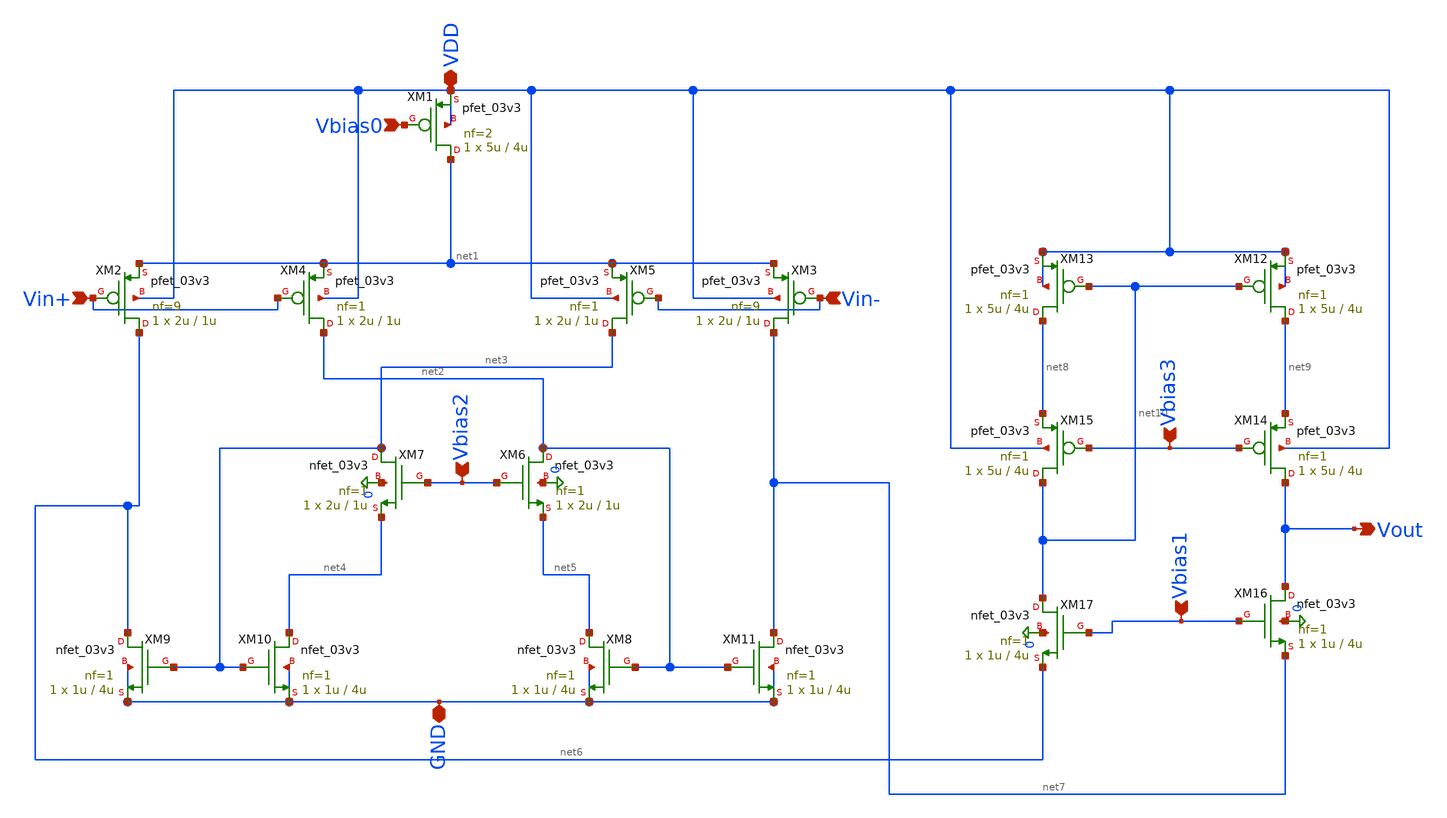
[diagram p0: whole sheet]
** sch_path: analog/folded_cascode_OTA.sch
**.subckt folded_cascode_OTA VDD Vbias0 Vin+ Vin- Vbias1 Vout Vbias3 Vbias2 GND
*.iopin VDD
*.ipin Vbias0
*.ipin Vin+
*.ipin Vin-
*.ipin Vbias1
*.opin Vout
*.ipin Vbias3
*.ipin Vbias2
*.iopin GND
XM1 net1 Vbias0 VDD VDD pfet_03v3 L=4u W=5u nf=2 ad='int((nf+1)/2) * W/nf * 0.18u' as='int((nf+2)/2) * W/nf * 0.18u'
+ pd='2*int((nf+1)/2) * (W/nf + 0.18u)' ps='2*int((nf+2)/2) * (W/nf + 0.18u)' nrd='0.18u / W' nrs='0.18u / W'
+ sa=0 sb=0 sd=0 m=1
XM2 net6 Vin+ net1 VDD pfet_03v3 L=1u W=2u nf=9 ad='int((nf+1)/2) * W/nf * 0.18u' as='int((nf+2)/2) * W/nf * 0.18u'
+ pd='2*int((nf+1)/2) * (W/nf + 0.18u)' ps='2*int((nf+2)/2) * (W/nf + 0.18u)' nrd='0.18u / W' nrs='0.18u / W'
+ sa=0 sb=0 sd=0 m=1
XM3 net7 Vin- net1 VDD pfet_03v3 L=1u W=2u nf=9 ad='int((nf+1)/2) * W/nf * 0.18u' as='int((nf+2)/2) * W/nf * 0.18u'
+ pd='2*int((nf+1)/2) * (W/nf + 0.18u)' ps='2*int((nf+2)/2) * (W/nf + 0.18u)' nrd='0.18u / W' nrs='0.18u / W'
+ sa=0 sb=0 sd=0 m=1
XM4 net2 Vin+ net1 VDD pfet_03v3 L=1u W=2u nf=1 ad='int((nf+1)/2) * W/nf * 0.18u' as='int((nf+2)/2) * W/nf * 0.18u'
+ pd='2*int((nf+1)/2) * (W/nf + 0.18u)' ps='2*int((nf+2)/2) * (W/nf + 0.18u)' nrd='0.18u / W' nrs='0.18u / W'
+ sa=0 sb=0 sd=0 m=1
XM5 net3 Vin- net1 VDD pfet_03v3 L=1u W=2u nf=1 ad='int((nf+1)/2) * W/nf * 0.18u' as='int((nf+2)/2) * W/nf * 0.18u'
+ pd='2*int((nf+1)/2) * (W/nf + 0.18u)' ps='2*int((nf+2)/2) * (W/nf + 0.18u)' nrd='0.18u / W' nrs='0.18u / W'
+ sa=0 sb=0 sd=0 m=1
XM6 net2 Vbias2 net5 0 nfet_03v3 L=1u W=2u nf=1 ad='int((nf+1)/2) * W/nf * 0.18u' as='int((nf+2)/2) * W/nf * 0.18u'
+ pd='2*int((nf+1)/2) * (W/nf + 0.18u)' ps='2*int((nf+2)/2) * (W/nf + 0.18u)' nrd='0.18u / W' nrs='0.18u / W'
+ sa=0 sb=0 sd=0 m=1
XM7 net3 Vbias2 net4 0 nfet_03v3 L=1u W=2u nf=1 ad='int((nf+1)/2) * W/nf * 0.18u' as='int((nf+2)/2) * W/nf * 0.18u'
+ pd='2*int((nf+1)/2) * (W/nf + 0.18u)' ps='2*int((nf+2)/2) * (W/nf + 0.18u)' nrd='0.18u / W' nrs='0.18u / W'
+ sa=0 sb=0 sd=0 m=1
XM8 net5 net2 GND GND nfet_03v3 L=4u W=1u nf=1 ad='int((nf+1)/2) * W/nf * 0.18u' as='int((nf+2)/2) * W/nf * 0.18u'
+ pd='2*int((nf+1)/2) * (W/nf + 0.18u)' ps='2*int((nf+2)/2) * (W/nf + 0.18u)' nrd='0.18u / W' nrs='0.18u / W'
+ sa=0 sb=0 sd=0 m=1
XM9 net6 net3 GND GND nfet_03v3 L=4u W=1u nf=1 ad='int((nf+1)/2) * W/nf * 0.18u' as='int((nf+2)/2) * W/nf * 0.18u'
+ pd='2*int((nf+1)/2) * (W/nf + 0.18u)' ps='2*int((nf+2)/2) * (W/nf + 0.18u)' nrd='0.18u / W' nrs='0.18u / W'
+ sa=0 sb=0 sd=0 m=1
XM10 net4 net3 GND GND nfet_03v3 L=4u W=1u nf=1 ad='int((nf+1)/2) * W/nf * 0.18u' as='int((nf+2)/2) * W/nf * 0.18u'
+ pd='2*int((nf+1)/2) * (W/nf + 0.18u)' ps='2*int((nf+2)/2) * (W/nf + 0.18u)' nrd='0.18u / W' nrs='0.18u / W'
+ sa=0 sb=0 sd=0 m=1
XM11 net7 net2 GND GND nfet_03v3 L=4u W=1u nf=1 ad='int((nf+1)/2) * W/nf * 0.18u' as='int((nf+2)/2) * W/nf * 0.18u'
+ pd='2*int((nf+1)/2) * (W/nf + 0.18u)' ps='2*int((nf+2)/2) * (W/nf + 0.18u)' nrd='0.18u / W' nrs='0.18u / W'
+ sa=0 sb=0 sd=0 m=1
XM12 net9 net10 VDD VDD pfet_03v3 L=4u W=5u nf=1 ad='int((nf+1)/2) * W/nf * 0.18u' as='int((nf+2)/2) * W/nf * 0.18u'
+ pd='2*int((nf+1)/2) * (W/nf + 0.18u)' ps='2*int((nf+2)/2) * (W/nf + 0.18u)' nrd='0.18u / W' nrs='0.18u / W'
+ sa=0 sb=0 sd=0 m=1
XM13 net8 net10 VDD VDD pfet_03v3 L=4u W=5u nf=1 ad='int((nf+1)/2) * W/nf * 0.18u' as='int((nf+2)/2) * W/nf * 0.18u'
+ pd='2*int((nf+1)/2) * (W/nf + 0.18u)' ps='2*int((nf+2)/2) * (W/nf + 0.18u)' nrd='0.18u / W' nrs='0.18u / W'
+ sa=0 sb=0 sd=0 m=1
XM14 Vout Vbias3 net9 VDD pfet_03v3 L=4u W=5u nf=1 ad='int((nf+1)/2) * W/nf * 0.18u' as='int((nf+2)/2) * W/nf * 0.18u'
+ pd='2*int((nf+1)/2) * (W/nf + 0.18u)' ps='2*int((nf+2)/2) * (W/nf + 0.18u)' nrd='0.18u / W' nrs='0.18u / W'
+ sa=0 sb=0 sd=0 m=1
XM15 net10 Vbias3 net8 VDD pfet_03v3 L=4u W=5u nf=1 ad='int((nf+1)/2) * W/nf * 0.18u' as='int((nf+2)/2) * W/nf * 0.18u'
+ pd='2*int((nf+1)/2) * (W/nf + 0.18u)' ps='2*int((nf+2)/2) * (W/nf + 0.18u)' nrd='0.18u / W' nrs='0.18u / W'
+ sa=0 sb=0 sd=0 m=1
XM16 Vout Vbias1 net7 0 nfet_03v3 L=4u W=1u nf=1 ad='int((nf+1)/2) * W/nf * 0.18u' as='int((nf+2)/2) * W/nf * 0.18u'
+ pd='2*int((nf+1)/2) * (W/nf + 0.18u)' ps='2*int((nf+2)/2) * (W/nf + 0.18u)' nrd='0.18u / W' nrs='0.18u / W'
+ sa=0 sb=0 sd=0 m=1
XM17 net10 Vbias1 net6 0 nfet_03v3 L=4u W=1u nf=1 ad='int((nf+1)/2) * W/nf * 0.18u' as='int((nf+2)/2) * W/nf * 0.18u'
+ pd='2*int((nf+1)/2) * (W/nf + 0.18u)' ps='2*int((nf+2)/2) * (W/nf + 0.18u)' nrd='0.18u / W' nrs='0.18u / W'
+ sa=0 sb=0 sd=0 m=1
**.ends
.end
